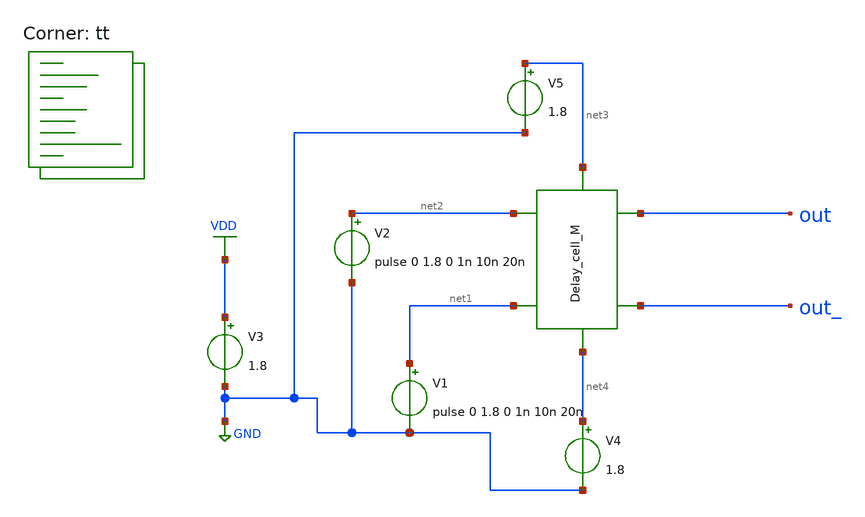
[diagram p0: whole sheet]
** sch_path: untitled-2.sch
**.subckt untitled-2
V1 net1 GND pulse 0 1.8 0 1n 10n 20n
V2 net2 GND pulse 0 1.8 0 1n 10n 20n
V3 VDD GND 1.8
V4 net4 GND 1.8
V5 net3 GND 1.8
**** begin user architecture code



.tran 1p 10n
.probe I(x1)
.save all

.lib $::SKYWATER_MODELS/sky130.lib.spice tt
**** end user architecture code
**.ends
.GLOBAL VDD
.GLOBAL GND
.end
